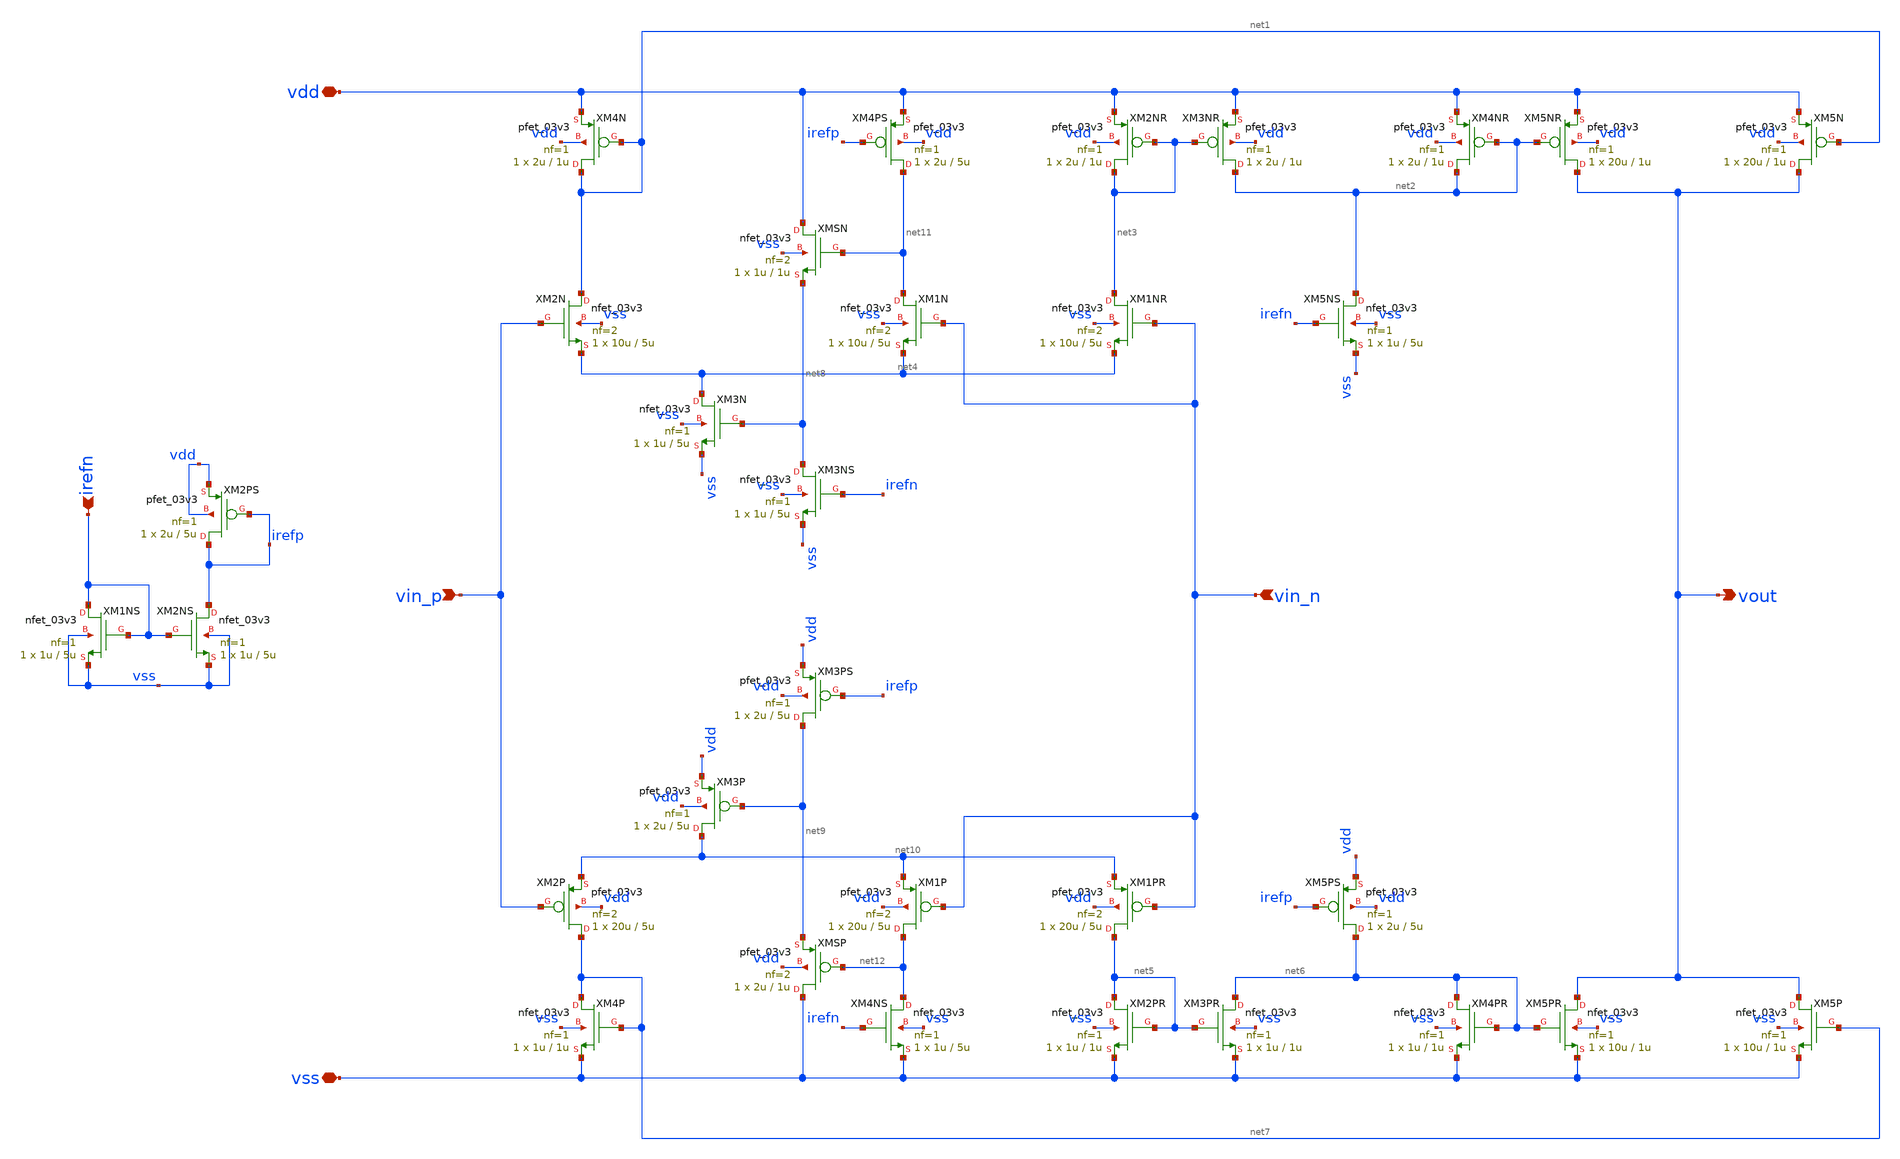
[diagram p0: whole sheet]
** sch_path: Tobias/2026 07 15 Intermediate Results/analogbuffer/analogbuffer-openloop.sch
**.subckt analogbuffer-openloop vdd vss vin_p vout irefn vin_n
*.iopin vdd
*.iopin vss
*.ipin vin_p
*.opin vout
*.ipin irefn
*.ipin vin_n
XM2P net7 vin_p net10 vdd pfet_03v3 L=5u W=20u nf=2 ad='int((nf+1)/2) * W/nf * 0.18u' as='int((nf+2)/2) * W/nf * 0.18u'
+ pd='2*int((nf+1)/2) * (W/nf + 0.18u)' ps='2*int((nf+2)/2) * (W/nf + 0.18u)' nrd='0.18u / W' nrs='0.18u / W'
+ sa=0 sb=0 sd=0 m=1
XM2N net1 vin_p net4 vss nfet_03v3 L=5u W=10u nf=2 ad='int((nf+1)/2) * W/nf * 0.18u' as='int((nf+2)/2) * W/nf * 0.18u'
+ pd='2*int((nf+1)/2) * (W/nf + 0.18u)' ps='2*int((nf+2)/2) * (W/nf + 0.18u)' nrd='0.18u / W' nrs='0.18u / W'
+ sa=0 sb=0 sd=0 m=1
XM3N net4 net8 vss vss nfet_03v3 L=5u W=1u nf=1 ad='int((nf+1)/2) * W/nf * 0.18u' as='int((nf+2)/2) * W/nf * 0.18u'
+ pd='2*int((nf+1)/2) * (W/nf + 0.18u)' ps='2*int((nf+2)/2) * (W/nf + 0.18u)' nrd='0.18u / W' nrs='0.18u / W'
+ sa=0 sb=0 sd=0 m=1
XM1NR net3 vin_n net4 vss nfet_03v3 L=5u W=10u nf=2 ad='int((nf+1)/2) * W/nf * 0.18u' as='int((nf+2)/2) * W/nf * 0.18u'
+ pd='2*int((nf+1)/2) * (W/nf + 0.18u)' ps='2*int((nf+2)/2) * (W/nf + 0.18u)' nrd='0.18u / W' nrs='0.18u / W'
+ sa=0 sb=0 sd=0 m=1
XM2NR net3 net3 vdd vdd pfet_03v3 L=1u W=2u nf=1 ad='int((nf+1)/2) * W/nf * 0.18u' as='int((nf+2)/2) * W/nf * 0.18u'
+ pd='2*int((nf+1)/2) * (W/nf + 0.18u)' ps='2*int((nf+2)/2) * (W/nf + 0.18u)' nrd='0.18u / W' nrs='0.18u / W'
+ sa=0 sb=0 sd=0 m=1
XM3NR net2 net3 vdd vdd pfet_03v3 L=1u W=2u nf=1 ad='int((nf+1)/2) * W/nf * 0.18u' as='int((nf+2)/2) * W/nf * 0.18u'
+ pd='2*int((nf+1)/2) * (W/nf + 0.18u)' ps='2*int((nf+2)/2) * (W/nf + 0.18u)' nrd='0.18u / W' nrs='0.18u / W'
+ sa=0 sb=0 sd=0 m=1
XM4NR net2 net2 vdd vdd pfet_03v3 L=1u W=2u nf=1 ad='int((nf+1)/2) * W/nf * 0.18u' as='int((nf+2)/2) * W/nf * 0.18u'
+ pd='2*int((nf+1)/2) * (W/nf + 0.18u)' ps='2*int((nf+2)/2) * (W/nf + 0.18u)' nrd='0.18u / W' nrs='0.18u / W'
+ sa=0 sb=0 sd=0 m=1
XM5NR vout net2 vdd vdd pfet_03v3 L=1u W=20u nf=1 ad='int((nf+1)/2) * W/nf * 0.18u' as='int((nf+2)/2) * W/nf * 0.18u'
+ pd='2*int((nf+1)/2) * (W/nf + 0.18u)' ps='2*int((nf+2)/2) * (W/nf + 0.18u)' nrd='0.18u / W' nrs='0.18u / W'
+ sa=0 sb=0 sd=0 m=1
XM5N vout net1 vdd vdd pfet_03v3 L=1u W=20u nf=1 ad='int((nf+1)/2) * W/nf * 0.18u' as='int((nf+2)/2) * W/nf * 0.18u'
+ pd='2*int((nf+1)/2) * (W/nf + 0.18u)' ps='2*int((nf+2)/2) * (W/nf + 0.18u)' nrd='0.18u / W' nrs='0.18u / W'
+ sa=0 sb=0 sd=0 m=1
XM4N net1 net1 vdd vdd pfet_03v3 L=1u W=2u nf=1 ad='int((nf+1)/2) * W/nf * 0.18u' as='int((nf+2)/2) * W/nf * 0.18u'
+ pd='2*int((nf+1)/2) * (W/nf + 0.18u)' ps='2*int((nf+2)/2) * (W/nf + 0.18u)' nrd='0.18u / W' nrs='0.18u / W'
+ sa=0 sb=0 sd=0 m=1
XM5NS net2 irefn vss vss nfet_03v3 L=5u W=1u nf=1 ad='int((nf+1)/2) * W/nf * 0.18u' as='int((nf+2)/2) * W/nf * 0.18u'
+ pd='2*int((nf+1)/2) * (W/nf + 0.18u)' ps='2*int((nf+2)/2) * (W/nf + 0.18u)' nrd='0.18u / W' nrs='0.18u / W'
+ sa=0 sb=0 sd=0 m=1
XM1PR net5 vin_n net10 vdd pfet_03v3 L=5u W=20u nf=2 ad='int((nf+1)/2) * W/nf * 0.18u' as='int((nf+2)/2) * W/nf * 0.18u'
+ pd='2*int((nf+1)/2) * (W/nf + 0.18u)' ps='2*int((nf+2)/2) * (W/nf + 0.18u)' nrd='0.18u / W' nrs='0.18u / W'
+ sa=0 sb=0 sd=0 m=1
XM3P net10 net9 vdd vdd pfet_03v3 L=5u W=2u nf=1 ad='int((nf+1)/2) * W/nf * 0.18u' as='int((nf+2)/2) * W/nf * 0.18u'
+ pd='2*int((nf+1)/2) * (W/nf + 0.18u)' ps='2*int((nf+2)/2) * (W/nf + 0.18u)' nrd='0.18u / W' nrs='0.18u / W'
+ sa=0 sb=0 sd=0 m=1
XM2PR net5 net5 vss vss nfet_03v3 L=1u W=1u nf=1 ad='int((nf+1)/2) * W/nf * 0.18u' as='int((nf+2)/2) * W/nf * 0.18u'
+ pd='2*int((nf+1)/2) * (W/nf + 0.18u)' ps='2*int((nf+2)/2) * (W/nf + 0.18u)' nrd='0.18u / W' nrs='0.18u / W'
+ sa=0 sb=0 sd=0 m=1
XM3PR net6 net5 vss vss nfet_03v3 L=1u W=1u nf=1 ad='int((nf+1)/2) * W/nf * 0.18u' as='int((nf+2)/2) * W/nf * 0.18u'
+ pd='2*int((nf+1)/2) * (W/nf + 0.18u)' ps='2*int((nf+2)/2) * (W/nf + 0.18u)' nrd='0.18u / W' nrs='0.18u / W'
+ sa=0 sb=0 sd=0 m=1
XM4PR net6 net6 vss vss nfet_03v3 L=1u W=1u nf=1 ad='int((nf+1)/2) * W/nf * 0.18u' as='int((nf+2)/2) * W/nf * 0.18u'
+ pd='2*int((nf+1)/2) * (W/nf + 0.18u)' ps='2*int((nf+2)/2) * (W/nf + 0.18u)' nrd='0.18u / W' nrs='0.18u / W'
+ sa=0 sb=0 sd=0 m=1
XM5PR vout net6 vss vss nfet_03v3 L=1u W=10u nf=1 ad='int((nf+1)/2) * W/nf * 0.18u' as='int((nf+2)/2) * W/nf * 0.18u'
+ pd='2*int((nf+1)/2) * (W/nf + 0.18u)' ps='2*int((nf+2)/2) * (W/nf + 0.18u)' nrd='0.18u / W' nrs='0.18u / W'
+ sa=0 sb=0 sd=0 m=1
XM5PS net6 irefp vdd vdd pfet_03v3 L=5u W=2u nf=1 ad='int((nf+1)/2) * W/nf * 0.18u' as='int((nf+2)/2) * W/nf * 0.18u'
+ pd='2*int((nf+1)/2) * (W/nf + 0.18u)' ps='2*int((nf+2)/2) * (W/nf + 0.18u)' nrd='0.18u / W' nrs='0.18u / W'
+ sa=0 sb=0 sd=0 m=1
XM5P vout net7 vss vss nfet_03v3 L=1u W=10u nf=1 ad='int((nf+1)/2) * W/nf * 0.18u' as='int((nf+2)/2) * W/nf * 0.18u'
+ pd='2*int((nf+1)/2) * (W/nf + 0.18u)' ps='2*int((nf+2)/2) * (W/nf + 0.18u)' nrd='0.18u / W' nrs='0.18u / W'
+ sa=0 sb=0 sd=0 m=1
XM4P net7 net7 vss vss nfet_03v3 L=1u W=1u nf=1 ad='int((nf+1)/2) * W/nf * 0.18u' as='int((nf+2)/2) * W/nf * 0.18u'
+ pd='2*int((nf+1)/2) * (W/nf + 0.18u)' ps='2*int((nf+2)/2) * (W/nf + 0.18u)' nrd='0.18u / W' nrs='0.18u / W'
+ sa=0 sb=0 sd=0 m=1
XM2NS irefp irefn vss vss nfet_03v3 L=5u W=1u nf=1 ad='int((nf+1)/2) * W/nf * 0.18u' as='int((nf+2)/2) * W/nf * 0.18u'
+ pd='2*int((nf+1)/2) * (W/nf + 0.18u)' ps='2*int((nf+2)/2) * (W/nf + 0.18u)' nrd='0.18u / W' nrs='0.18u / W'
+ sa=0 sb=0 sd=0 m=1
XM1NS irefn irefn vss vss nfet_03v3 L=5u W=1u nf=1 ad='int((nf+1)/2) * W/nf * 0.18u' as='int((nf+2)/2) * W/nf * 0.18u'
+ pd='2*int((nf+1)/2) * (W/nf + 0.18u)' ps='2*int((nf+2)/2) * (W/nf + 0.18u)' nrd='0.18u / W' nrs='0.18u / W'
+ sa=0 sb=0 sd=0 m=1
XM2PS irefp irefp vdd vdd pfet_03v3 L=5u W=2u nf=1 ad='int((nf+1)/2) * W/nf * 0.18u' as='int((nf+2)/2) * W/nf * 0.18u'
+ pd='2*int((nf+1)/2) * (W/nf + 0.18u)' ps='2*int((nf+2)/2) * (W/nf + 0.18u)' nrd='0.18u / W' nrs='0.18u / W'
+ sa=0 sb=0 sd=0 m=1
XMSN vdd net11 net8 vss nfet_03v3 L=1u W=1u nf=2 ad='int((nf+1)/2) * W/nf * 0.18u' as='int((nf+2)/2) * W/nf * 0.18u'
+ pd='2*int((nf+1)/2) * (W/nf + 0.18u)' ps='2*int((nf+2)/2) * (W/nf + 0.18u)' nrd='0.18u / W' nrs='0.18u / W'
+ sa=0 sb=0 sd=0 m=1
XM3NS net8 irefn vss vss nfet_03v3 L=5u W=1u nf=1 ad='int((nf+1)/2) * W/nf * 0.18u' as='int((nf+2)/2) * W/nf * 0.18u'
+ pd='2*int((nf+1)/2) * (W/nf + 0.18u)' ps='2*int((nf+2)/2) * (W/nf + 0.18u)' nrd='0.18u / W' nrs='0.18u / W'
+ sa=0 sb=0 sd=0 m=1
XM1N net11 vin_n net4 vss nfet_03v3 L=5u W=10u nf=2 ad='int((nf+1)/2) * W/nf * 0.18u' as='int((nf+2)/2) * W/nf * 0.18u'
+ pd='2*int((nf+1)/2) * (W/nf + 0.18u)' ps='2*int((nf+2)/2) * (W/nf + 0.18u)' nrd='0.18u / W' nrs='0.18u / W'
+ sa=0 sb=0 sd=0 m=1
XM4PS net11 irefp vdd vdd pfet_03v3 L=5u W=2u nf=1 ad='int((nf+1)/2) * W/nf * 0.18u' as='int((nf+2)/2) * W/nf * 0.18u'
+ pd='2*int((nf+1)/2) * (W/nf + 0.18u)' ps='2*int((nf+2)/2) * (W/nf + 0.18u)' nrd='0.18u / W' nrs='0.18u / W'
+ sa=0 sb=0 sd=0 m=1
XM3PS net9 irefp vdd vdd pfet_03v3 L=5u W=2u nf=1 ad='int((nf+1)/2) * W/nf * 0.18u' as='int((nf+2)/2) * W/nf * 0.18u'
+ pd='2*int((nf+1)/2) * (W/nf + 0.18u)' ps='2*int((nf+2)/2) * (W/nf + 0.18u)' nrd='0.18u / W' nrs='0.18u / W'
+ sa=0 sb=0 sd=0 m=1
XM1P net12 vin_n net10 vdd pfet_03v3 L=5u W=20u nf=2 ad='int((nf+1)/2) * W/nf * 0.18u' as='int((nf+2)/2) * W/nf * 0.18u'
+ pd='2*int((nf+1)/2) * (W/nf + 0.18u)' ps='2*int((nf+2)/2) * (W/nf + 0.18u)' nrd='0.18u / W' nrs='0.18u / W'
+ sa=0 sb=0 sd=0 m=1
XM4NS net12 irefn vss vss nfet_03v3 L=5u W=1u nf=1 ad='int((nf+1)/2) * W/nf * 0.18u' as='int((nf+2)/2) * W/nf * 0.18u'
+ pd='2*int((nf+1)/2) * (W/nf + 0.18u)' ps='2*int((nf+2)/2) * (W/nf + 0.18u)' nrd='0.18u / W' nrs='0.18u / W'
+ sa=0 sb=0 sd=0 m=1
XMSP vss net12 net9 vdd pfet_03v3 L=1u W=2u nf=2 ad='int((nf+1)/2) * W/nf * 0.18u' as='int((nf+2)/2) * W/nf * 0.18u'
+ pd='2*int((nf+1)/2) * (W/nf + 0.18u)' ps='2*int((nf+2)/2) * (W/nf + 0.18u)' nrd='0.18u / W' nrs='0.18u / W'
+ sa=0 sb=0 sd=0 m=1
**.ends
.end
